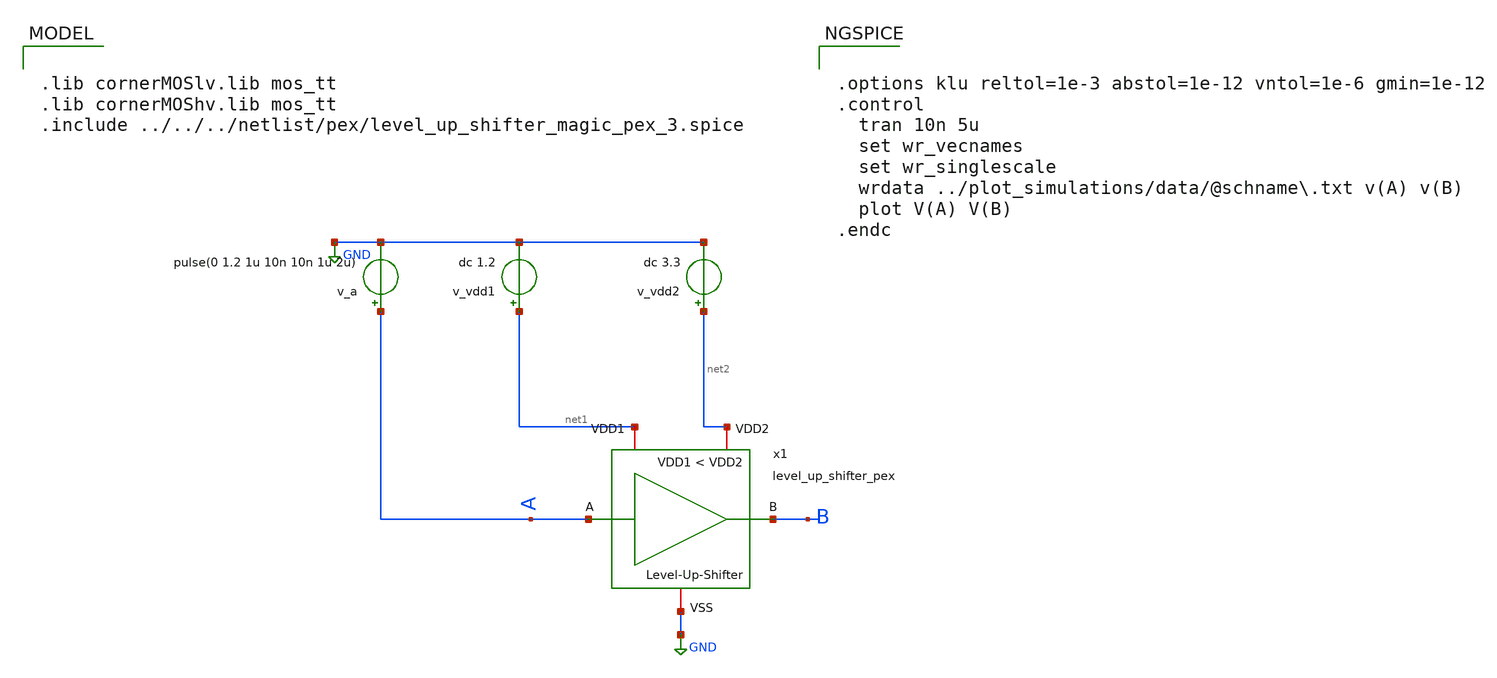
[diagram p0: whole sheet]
** sch_path: macros/level_shifter/testbenches/xschem/level_up_shifter_tb_tran.sch
**.subckt level_up_shifter_tb_tran
v_a A GND pulse(0 1.2 1u 10n 10n 1u 2u)
v_vdd1 net1 GND dc 1.2
v_vdd2 net2 GND dc 3.3
x1 net2 A B GND net1 level_up_shifter_pex
**** begin user architecture code

.lib cornerMOSlv.lib mos_tt
.lib cornerMOShv.lib mos_tt
.include ../../../netlist/pex/level_up_shifter_magic_pex_3.spice



.options klu reltol=1e-3 abstol=1e-12 vntol=1e-6 gmin=1e-12
.control
  tran 10n 5u
  set wr_vecnames
  set wr_singlescale
  wrdata ../plot_simulations/data/@schname\.txt v(A) v(B)
  plot V(A) V(B)
.endc


**** end user architecture code
**.ends
.GLOBAL GND
.end
